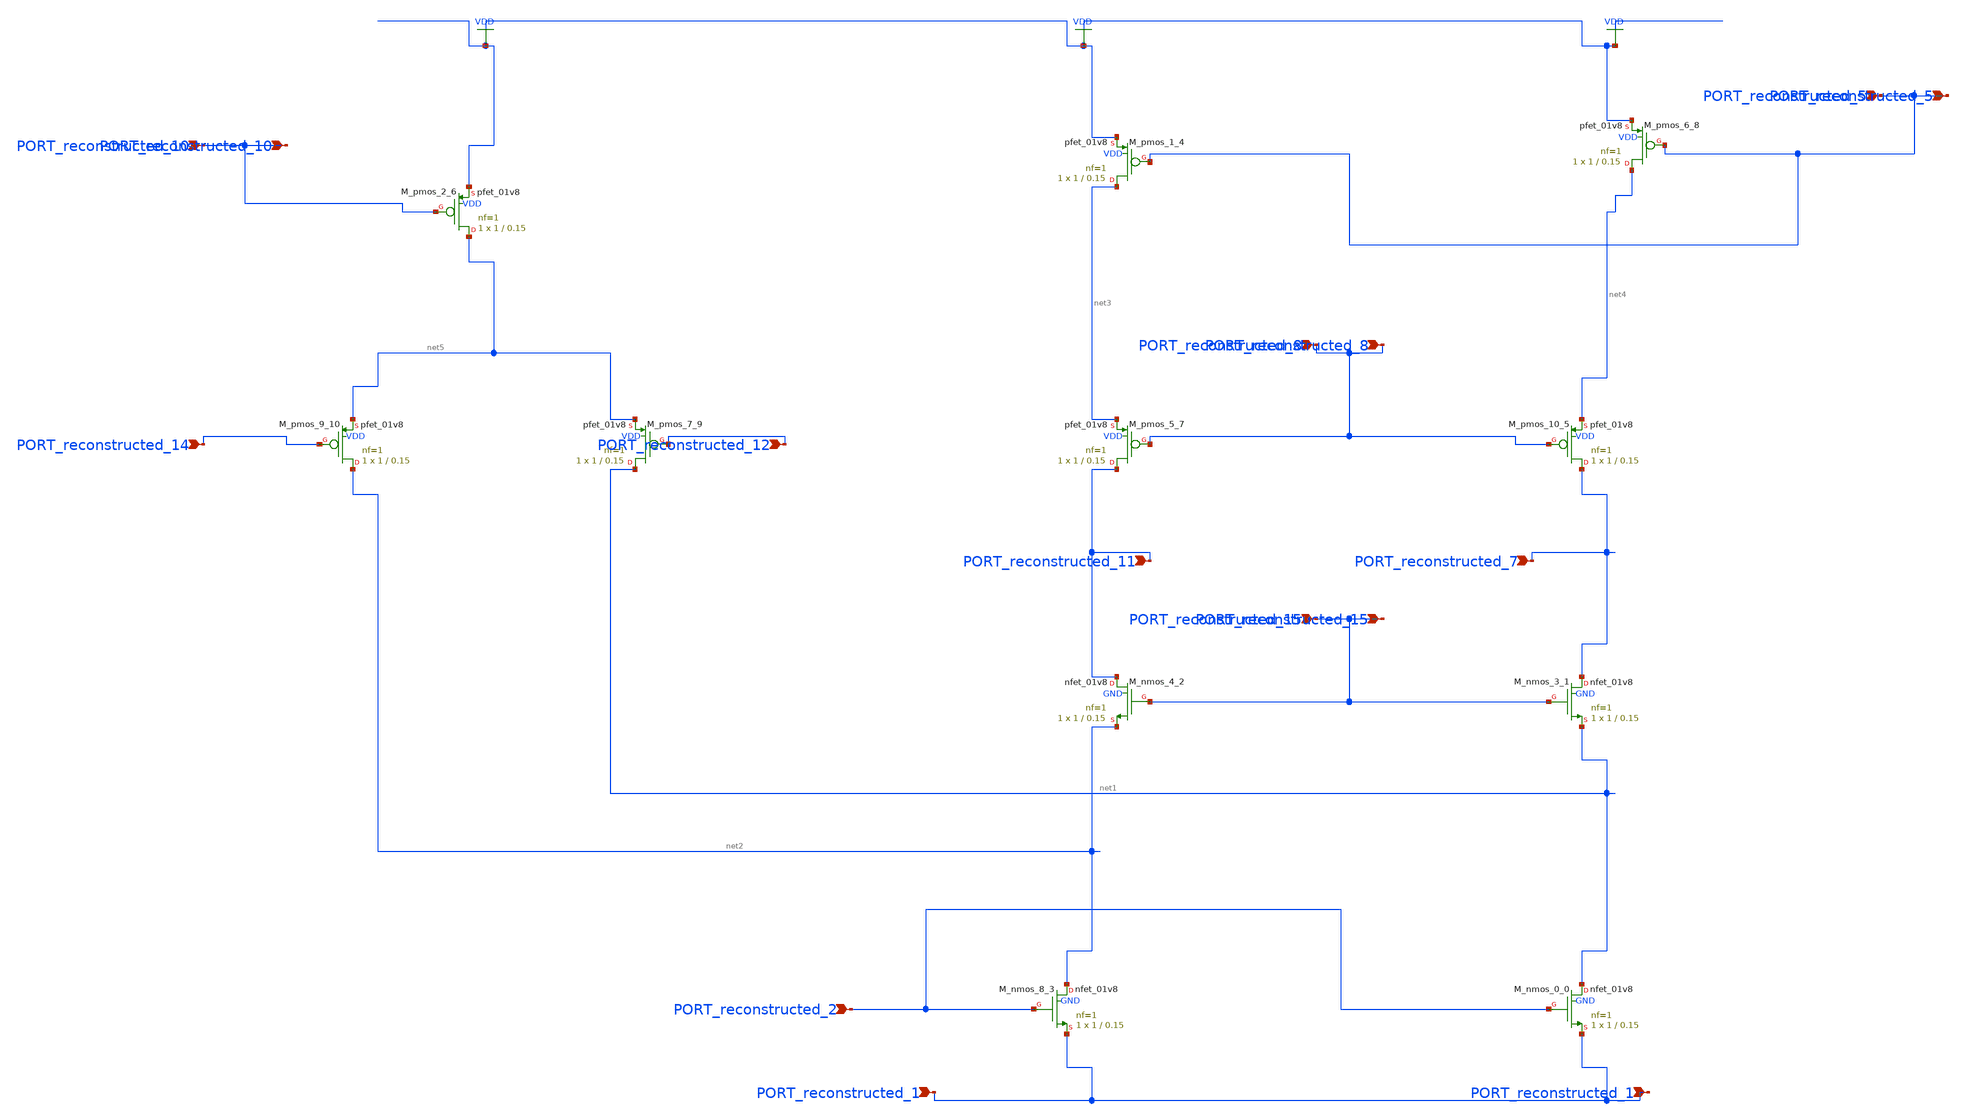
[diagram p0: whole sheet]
** sch_path: schematics/Image2Net/091.sch
**.subckt 091 PORT_reconstructed_12 PORT_reconstructed_14 PORT_reconstructed_7 PORT_reconstructed_11
*+ PORT_reconstructed_2 PORT_reconstructed_10 PORT_reconstructed_1 PORT_reconstructed_15 PORT_reconstructed_10
*+ PORT_reconstructed_5 PORT_reconstructed_8 PORT_reconstructed_8 PORT_reconstructed_5 PORT_reconstructed_15
*+ PORT_reconstructed_1
*.ipin PORT_reconstructed_12
*.ipin PORT_reconstructed_14
*.ipin PORT_reconstructed_7
*.ipin PORT_reconstructed_11
*.ipin PORT_reconstructed_2
*.ipin PORT_reconstructed_10
*.ipin PORT_reconstructed_1
*.ipin PORT_reconstructed_15
*.ipin PORT_reconstructed_10
*.ipin PORT_reconstructed_5
*.ipin PORT_reconstructed_8
*.ipin PORT_reconstructed_8
*.ipin PORT_reconstructed_5
*.ipin PORT_reconstructed_15
*.ipin PORT_reconstructed_1
XM_nmos_0_0 net1 PORT_reconstructed_2 PORT_reconstructed_1 GND sky130_fd_pr__nfet_01v8 L=0.15 W=1 nf=1
+ ad='int((1 + 1)/2) * 1 / 1 * 0.29' as='int((1 + 2)/2) * 1 / 1 * 0.29' pd='2*int((1 + 1)/2) * (1 / 1 + 0.29)'
+ ps='2*int((1 + 2)/2) * (1 / 1 + 0.29)' nrd='0.29 / 1 ' nrs='0.29 / 1 ' sa=0 sb=0 sd=0 mult=1 m=1
XM_nmos_3_1 PORT_reconstructed_7 PORT_reconstructed_15 net1 GND sky130_fd_pr__nfet_01v8 L=0.15 W=1 nf=1
+ ad='int((1 + 1)/2) * 1 / 1 * 0.29' as='int((1 + 2)/2) * 1 / 1 * 0.29' pd='2*int((1 + 1)/2) * (1 / 1 + 0.29)'
+ ps='2*int((1 + 2)/2) * (1 / 1 + 0.29)' nrd='0.29 / 1 ' nrs='0.29 / 1 ' sa=0 sb=0 sd=0 mult=1 m=1
XM_nmos_4_2 PORT_reconstructed_11 PORT_reconstructed_15 net2 GND sky130_fd_pr__nfet_01v8 L=0.15 W=1 nf=1
+ ad='int((1 + 1)/2) * 1 / 1 * 0.29' as='int((1 + 2)/2) * 1 / 1 * 0.29' pd='2*int((1 + 1)/2) * (1 / 1 + 0.29)'
+ ps='2*int((1 + 2)/2) * (1 / 1 + 0.29)' nrd='0.29 / 1 ' nrs='0.29 / 1 ' sa=0 sb=0 sd=0 mult=1 m=1
XM_nmos_8_3 net2 PORT_reconstructed_2 PORT_reconstructed_1 GND sky130_fd_pr__nfet_01v8 L=0.15 W=1 nf=1
+ ad='int((1 + 1)/2) * 1 / 1 * 0.29' as='int((1 + 2)/2) * 1 / 1 * 0.29' pd='2*int((1 + 1)/2) * (1 / 1 + 0.29)'
+ ps='2*int((1 + 2)/2) * (1 / 1 + 0.29)' nrd='0.29 / 1 ' nrs='0.29 / 1 ' sa=0 sb=0 sd=0 mult=1 m=1
XM_pmos_1_4 net3 PORT_reconstructed_5 VDD VDD sky130_fd_pr__pfet_01v8 L=0.15 W=1 nf=1 ad='int((1 + 1)/2) * 1 / 1 * 0.29'
+ as='int((1 + 2)/2) * 1 / 1 * 0.29' pd='2*int((1 + 1)/2) * (1 / 1 + 0.29)' ps='2*int((1 + 2)/2) * (1 / 1 + 0.29)'
+ nrd='0.29 / 1 ' nrs='0.29 / 1 ' sa=0 sb=0 sd=0 mult=1 m=1
XM_pmos_10_5 PORT_reconstructed_7 PORT_reconstructed_8 net4 VDD sky130_fd_pr__pfet_01v8 L=0.15 W=1 nf=1
+ ad='int((1 + 1)/2) * 1 / 1 * 0.29' as='int((1 + 2)/2) * 1 / 1 * 0.29' pd='2*int((1 + 1)/2) * (1 / 1 + 0.29)'
+ ps='2*int((1 + 2)/2) * (1 / 1 + 0.29)' nrd='0.29 / 1 ' nrs='0.29 / 1 ' sa=0 sb=0 sd=0 mult=1 m=1
XM_pmos_2_6 net5 PORT_reconstructed_10 VDD VDD sky130_fd_pr__pfet_01v8 L=0.15 W=1 nf=1 ad='int((1 + 1)/2) * 1 / 1 * 0.29'
+ as='int((1 + 2)/2) * 1 / 1 * 0.29' pd='2*int((1 + 1)/2) * (1 / 1 + 0.29)' ps='2*int((1 + 2)/2) * (1 / 1 + 0.29)'
+ nrd='0.29 / 1 ' nrs='0.29 / 1 ' sa=0 sb=0 sd=0 mult=1 m=1
XM_pmos_5_7 PORT_reconstructed_11 PORT_reconstructed_8 net3 VDD sky130_fd_pr__pfet_01v8 L=0.15 W=1 nf=1
+ ad='int((1 + 1)/2) * 1 / 1 * 0.29' as='int((1 + 2)/2) * 1 / 1 * 0.29' pd='2*int((1 + 1)/2) * (1 / 1 + 0.29)'
+ ps='2*int((1 + 2)/2) * (1 / 1 + 0.29)' nrd='0.29 / 1 ' nrs='0.29 / 1 ' sa=0 sb=0 sd=0 mult=1 m=1
XM_pmos_6_8 net4 PORT_reconstructed_5 VDD VDD sky130_fd_pr__pfet_01v8 L=0.15 W=1 nf=1 ad='int((1 + 1)/2) * 1 / 1 * 0.29'
+ as='int((1 + 2)/2) * 1 / 1 * 0.29' pd='2*int((1 + 1)/2) * (1 / 1 + 0.29)' ps='2*int((1 + 2)/2) * (1 / 1 + 0.29)'
+ nrd='0.29 / 1 ' nrs='0.29 / 1 ' sa=0 sb=0 sd=0 mult=1 m=1
XM_pmos_7_9 net1 PORT_reconstructed_12 net5 VDD sky130_fd_pr__pfet_01v8 L=0.15 W=1 nf=1 ad='int((1 + 1)/2) * 1 / 1 * 0.29'
+ as='int((1 + 2)/2) * 1 / 1 * 0.29' pd='2*int((1 + 1)/2) * (1 / 1 + 0.29)' ps='2*int((1 + 2)/2) * (1 / 1 + 0.29)'
+ nrd='0.29 / 1 ' nrs='0.29 / 1 ' sa=0 sb=0 sd=0 mult=1 m=1
XM_pmos_9_10 net2 PORT_reconstructed_14 net5 VDD sky130_fd_pr__pfet_01v8 L=0.15 W=1 nf=1 ad='int((1 + 1)/2) * 1 / 1 * 0.29'
+ as='int((1 + 2)/2) * 1 / 1 * 0.29' pd='2*int((1 + 1)/2) * (1 / 1 + 0.29)' ps='2*int((1 + 2)/2) * (1 / 1 + 0.29)'
+ nrd='0.29 / 1 ' nrs='0.29 / 1 ' sa=0 sb=0 sd=0 mult=1 m=1
**.ends
.GLOBAL VDD
.end
